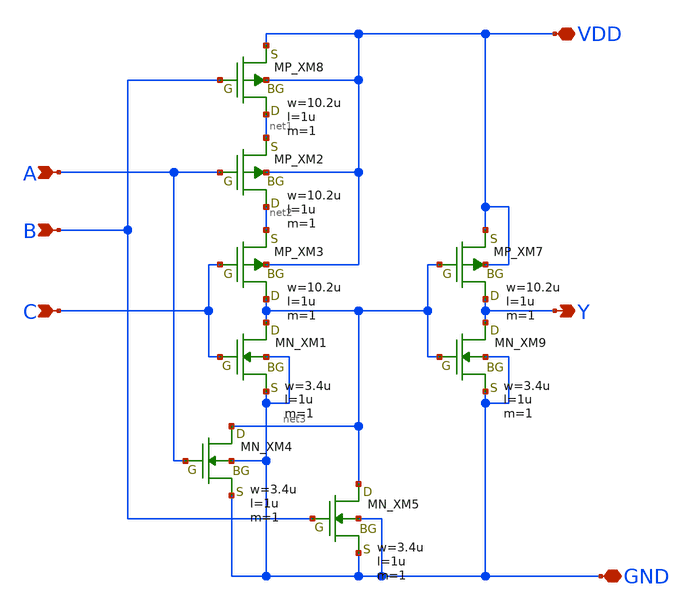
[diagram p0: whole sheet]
** sch_path: openIP62_rev1.0/IP62/Technology/tech/symbols/Xschem/IP62_5_stdcell/OR3.sch
**.subckt OR3 A B Y VDD GND C
*.ipin A
*.ipin B
*.opin Y
*.iopin VDD
*.iopin GND
*.ipin C
XM8 net1 B VDD VDD PMOS w=10.2u l=1u as=0 ad=0 ps=0 pd=0 nrd=0 nrs=0 m=1
XM2 net2 A net1 VDD PMOS w=10.2u l=1u as=0 ad=0 ps=0 pd=0 nrd=0 nrs=0 m=1
XM3 net3 C net2 VDD PMOS w=10.2u l=1u as=0 ad=0 ps=0 pd=0 nrd=0 nrs=0 m=1
XM7 Y net3 VDD VDD PMOS w=10.2u l=1u as=0 ad=0 ps=0 pd=0 nrd=0 nrs=0 m=1
XM9 Y net3 GND GND NMOS w=3.4u l=1u as=0 ad=0 ps=0 pd=0 nrd=0 nrs=0 m=1
XM1 net3 C GND GND NMOS w=3.4u l=1u as=0 ad=0 ps=0 pd=0 nrd=0 nrs=0 m=1
XM4 net3 A GND GND NMOS w=3.4u l=1u as=0 ad=0 ps=0 pd=0 nrd=0 nrs=0 m=1
XM5 net3 B GND GND NMOS w=3.4u l=1u as=0 ad=0 ps=0 pd=0 nrd=0 nrs=0 m=1
**.ends
.end
